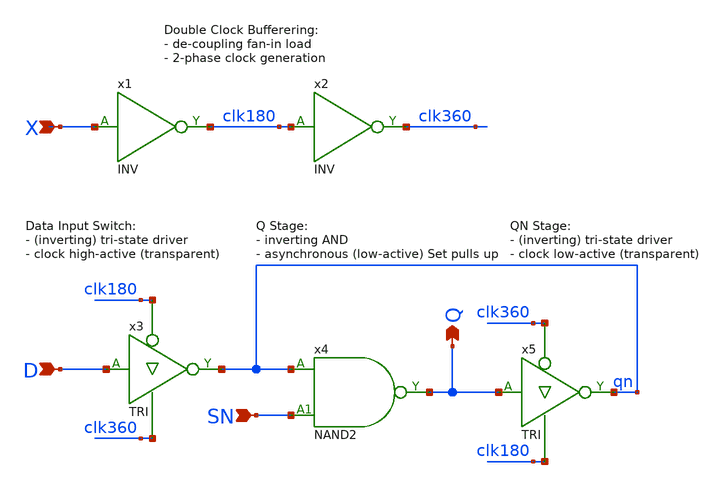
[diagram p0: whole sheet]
** sch_path: Sources/crafted/LATPS.sch
**.subckt LATPS X D Q SN
*.ipin X
*.ipin D
*.opin Q
*.ipin SN
x3 D clk180 clk360 qn VDD GND TRI Wmin=1.5u Lmin=1u g=2 m=1
x5 Q clk360 clk180 qn VDD GND TRI Wmin=1.5u Lmin=1u g=2 m=1
x4 qn SN Q VDD GND NAND2 Wmin=1.5u Lmin=1u g=2 m=1
x1 X clk180 VDD GND INV Wmin=1.5u Lmin=1u g=2 m=1
x2 clk180 clk360 VDD GND INV Wmin=1.5u Lmin=1u g=2 m=1
**.ends
.end
